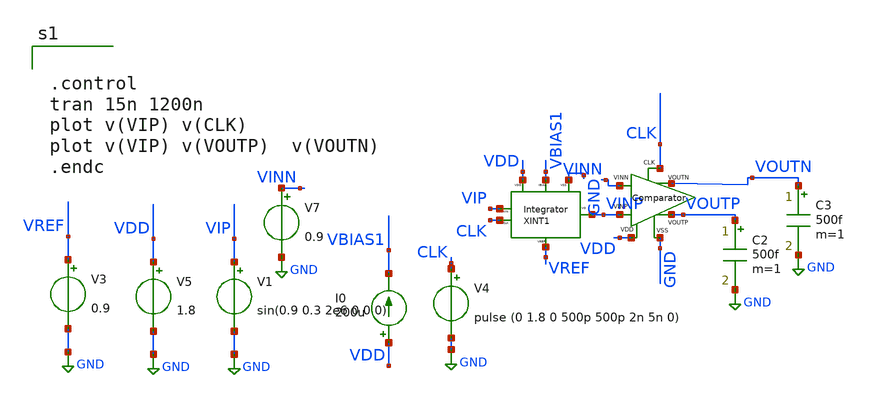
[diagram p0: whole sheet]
** sch_path: xschem/xschem_BGR_Top/Sigma_Delta/Integrator/Integrator_n_Comp_TB.sch
**.subckt Integrator_n_Comp_TB
V5 VDD GND 1.8
I0 VDD VBIAS1 200u
XINT1 VREF CLK VIP VINP VDD GND VBIAS1 Integrator
V3 VREF GND 0.9
V4 CLK GND pulse (0 1.8 0 500p 500p 2n 5n 0)
V1 VIP GND sin(0.9 0.3 2e6 0 0 0)
XCOMP1 VINN VINP VOUTN VOUTP CLK VDD GND Comparator
V7 VINN GND 0.9
C2 VOUTP GND 500f m=1
C3 VOUTN GND 500f m=1
**** begin user architecture code
** manual skywater pdks install (with patches applied)
* .lib $::SKYWATER_MODELS/models/sky130.lib.spice tt

** opencircuitdesign pdks install
.lib $::SKYWATER_MODELS/sky130.lib.spice tt




.control
tran 15n 1200n
plot v(VIP) v(CLK)
plot v(VIP) v(VOUTP)  v(VOUTN)
.endc

**** end user architecture code
**.ends

* expanding   symbol:  Sigma_Delta/Integrator/Integrator.sym # of pins=7
** sym_path: xschem/xschem_BGR_Top/Sigma_Delta/Integrator/Integrator.sym
** sch_path: xschem/xschem_BGR_Top/Sigma_Delta/Integrator/Integrator.sch
.subckt Integrator VREF CLK VIN VO VDD VSS IBIAS
*.iopin VDD
*.iopin VSS
*.iopin CLK
*.iopin IBIAS
*.iopin VREF
*.iopin VIN
*.iopin VO
XOpampM1 IBIAS VDD net1 VREF VSS VO OpampM
X1 VREF PH2 net1 VDD VSS PH1 VIN SC_Resistor
X2 PH2 VDD VSS PH1 CLK Non_over_clk
XC1 net1 VO sky130_fd_pr__cap_mim_m3_1 W=15 L=15 MF=1 m=1
.ends


* expanding   symbol:  Sigma_Delta/Comparator/Comparator.sym # of pins=7
** sym_path: xschem/xschem_BGR_Top/Sigma_Delta/Comparator/Comparator.sym
** sch_path: xschem/xschem_BGR_Top/Sigma_Delta/Comparator/Comparator.sch
.subckt Comparator VINN VINP VOUTN VOUTP CLK VDD VSS
*.iopin VDD
*.iopin VSS
*.iopin VOUTP
*.iopin VOUTN
*.iopin VINP
*.iopin VINN
*.iopin CLK
XM16 net1 net4 net2 VSS sky130_fd_pr__nfet_01v8 L=0.15 W=0.5 nf=1 ad='int((nf+1)/2) * W/nf * 0.29' as='int((nf+2)/2) * W/nf * 0.29'
+ pd='2*int((nf+1)/2) * (W/nf + 0.29)' ps='2*int((nf+2)/2) * (W/nf + 0.29)' nrd='0.29 / W' nrs='0.29 / W'
+ sa=0 sb=0 sd=0 mult=1 m=1
XM17 net1 net4 VDD VDD sky130_fd_pr__pfet_01v8 L=0.15 W=1 nf=1 ad='int((nf+1)/2) * W/nf * 0.29' as='int((nf+2)/2) * W/nf * 0.29'
+ pd='2*int((nf+1)/2) * (W/nf + 0.29)' ps='2*int((nf+2)/2) * (W/nf + 0.29)' nrd='0.29 / W' nrs='0.29 / W'
+ sa=0 sb=0 sd=0 mult=1 m=1
XM18 net2 VINN net3 VSS sky130_fd_pr__nfet_01v8 L=0.15 W=2 nf=1 ad='int((nf+1)/2) * W/nf * 0.29' as='int((nf+2)/2) * W/nf * 0.29'
+ pd='2*int((nf+1)/2) * (W/nf + 0.29)' ps='2*int((nf+2)/2) * (W/nf + 0.29)' nrd='0.29 / W' nrs='0.29 / W'
+ sa=0 sb=0 sd=0 mult=1 m=1
XM19 net1 CLK VDD VDD sky130_fd_pr__pfet_01v8 L=0.15 W=1 nf=1 ad='int((nf+1)/2) * W/nf * 0.29' as='int((nf+2)/2) * W/nf * 0.29'
+ pd='2*int((nf+1)/2) * (W/nf + 0.29)' ps='2*int((nf+2)/2) * (W/nf + 0.29)' nrd='0.29 / W' nrs='0.29 / W'
+ sa=0 sb=0 sd=0 mult=1 m=1
XM20 net2 CLK VDD VDD sky130_fd_pr__pfet_01v8 L=0.15 W=1 nf=1 ad='int((nf+1)/2) * W/nf * 0.29' as='int((nf+2)/2) * W/nf * 0.29'
+ pd='2*int((nf+1)/2) * (W/nf + 0.29)' ps='2*int((nf+2)/2) * (W/nf + 0.29)' nrd='0.29 / W' nrs='0.29 / W'
+ sa=0 sb=0 sd=0 mult=1 m=1
XM21 VOUTN net1 VSS VSS sky130_fd_pr__nfet_01v8 L=0.15 W=2 nf=1 ad='int((nf+1)/2) * W/nf * 0.29' as='int((nf+2)/2) * W/nf * 0.29'
+ pd='2*int((nf+1)/2) * (W/nf + 0.29)' ps='2*int((nf+2)/2) * (W/nf + 0.29)' nrd='0.29 / W' nrs='0.29 / W'
+ sa=0 sb=0 sd=0 mult=1 m=1
XM22 VOUTN net1 VDD VDD sky130_fd_pr__pfet_01v8 L=0.15 W=4 nf=1 ad='int((nf+1)/2) * W/nf * 0.29' as='int((nf+2)/2) * W/nf * 0.29'
+ pd='2*int((nf+1)/2) * (W/nf + 0.29)' ps='2*int((nf+2)/2) * (W/nf + 0.29)' nrd='0.29 / W' nrs='0.29 / W'
+ sa=0 sb=0 sd=0 mult=1 m=1
XM23 net4 net1 net5 VSS sky130_fd_pr__nfet_01v8 L=0.15 W=0.5 nf=1 ad='int((nf+1)/2) * W/nf * 0.29' as='int((nf+2)/2) * W/nf * 0.29'
+ pd='2*int((nf+1)/2) * (W/nf + 0.29)' ps='2*int((nf+2)/2) * (W/nf + 0.29)' nrd='0.29 / W' nrs='0.29 / W'
+ sa=0 sb=0 sd=0 mult=1 m=1
XM24 net4 net1 VDD VDD sky130_fd_pr__pfet_01v8 L=0.15 W=1 nf=1 ad='int((nf+1)/2) * W/nf * 0.29' as='int((nf+2)/2) * W/nf * 0.29'
+ pd='2*int((nf+1)/2) * (W/nf + 0.29)' ps='2*int((nf+2)/2) * (W/nf + 0.29)' nrd='0.29 / W' nrs='0.29 / W'
+ sa=0 sb=0 sd=0 mult=1 m=1
XM25 net5 VINP net3 VSS sky130_fd_pr__nfet_01v8 L=0.15 W=2 nf=1 ad='int((nf+1)/2) * W/nf * 0.29' as='int((nf+2)/2) * W/nf * 0.29'
+ pd='2*int((nf+1)/2) * (W/nf + 0.29)' ps='2*int((nf+2)/2) * (W/nf + 0.29)' nrd='0.29 / W' nrs='0.29 / W'
+ sa=0 sb=0 sd=0 mult=1 m=1
XM26 net4 CLK VDD VDD sky130_fd_pr__pfet_01v8 L=0.15 W=1 nf=1 ad='int((nf+1)/2) * W/nf * 0.29' as='int((nf+2)/2) * W/nf * 0.29'
+ pd='2*int((nf+1)/2) * (W/nf + 0.29)' ps='2*int((nf+2)/2) * (W/nf + 0.29)' nrd='0.29 / W' nrs='0.29 / W'
+ sa=0 sb=0 sd=0 mult=1 m=1
XM27 net5 CLK VDD VDD sky130_fd_pr__pfet_01v8 L=0.15 W=1 nf=1 ad='int((nf+1)/2) * W/nf * 0.29' as='int((nf+2)/2) * W/nf * 0.29'
+ pd='2*int((nf+1)/2) * (W/nf + 0.29)' ps='2*int((nf+2)/2) * (W/nf + 0.29)' nrd='0.29 / W' nrs='0.29 / W'
+ sa=0 sb=0 sd=0 mult=1 m=1
XM28 VOUTP net4 VSS VSS sky130_fd_pr__nfet_01v8 L=0.15 W=2 nf=1 ad='int((nf+1)/2) * W/nf * 0.29' as='int((nf+2)/2) * W/nf * 0.29'
+ pd='2*int((nf+1)/2) * (W/nf + 0.29)' ps='2*int((nf+2)/2) * (W/nf + 0.29)' nrd='0.29 / W' nrs='0.29 / W'
+ sa=0 sb=0 sd=0 mult=1 m=1
XM29 VOUTP net4 VDD VDD sky130_fd_pr__pfet_01v8 L=0.15 W=4 nf=1 ad='int((nf+1)/2) * W/nf * 0.29' as='int((nf+2)/2) * W/nf * 0.29'
+ pd='2*int((nf+1)/2) * (W/nf + 0.29)' ps='2*int((nf+2)/2) * (W/nf + 0.29)' nrd='0.29 / W' nrs='0.29 / W'
+ sa=0 sb=0 sd=0 mult=1 m=1
XM30 net3 CLK VSS VSS sky130_fd_pr__nfet_01v8 L=0.15 W=0.5 nf=1 ad='int((nf+1)/2) * W/nf * 0.29' as='int((nf+2)/2) * W/nf * 0.29'
+ pd='2*int((nf+1)/2) * (W/nf + 0.29)' ps='2*int((nf+2)/2) * (W/nf + 0.29)' nrd='0.29 / W' nrs='0.29 / W'
+ sa=0 sb=0 sd=0 mult=1 m=1
.ends


* expanding   symbol:  Sigma_Delta/Op_Amp/OpampM.sym # of pins=6
** sym_path: xschem/xschem_BGR_Top/Op_Amp/OpampM.sym
** sch_path: xschem/xschem_BGR_Top/Op_Amp/OpampM.sch
.subckt OpampM IBIAS VDD VN VP VSS VO
*.iopin VDD
*.iopin VSS
*.iopin VP
*.iopin VN
*.iopin VO
*.iopin IBIAS
XM1 net1 VN net3 VSS sky130_fd_pr__nfet_01v8 L=0.5 W=50 nf=10 ad='int((nf+1)/2) * W/nf * 0.29' as='int((nf+2)/2) * W/nf * 0.29'
+ pd='2*int((nf+1)/2) * (W/nf + 0.29)' ps='2*int((nf+2)/2) * (W/nf + 0.29)' nrd='0.29 / W' nrs='0.29 / W'
+ sa=0 sb=0 sd=0 mult=1 m=1
XM3 net1 net1 VDD VDD sky130_fd_pr__pfet_01v8_lvt L=0.5 W=60 nf=10 ad='int((nf+1)/2) * W/nf * 0.29' as='int((nf+2)/2) * W/nf * 0.29'
+ pd='2*int((nf+1)/2) * (W/nf + 0.29)' ps='2*int((nf+2)/2) * (W/nf + 0.29)' nrd='0.29 / W' nrs='0.29 / W'
+ sa=0 sb=0 sd=0 mult=1 m=1
XM2 net2 VP net3 VSS sky130_fd_pr__nfet_01v8 L=0.5 W=50 nf=10 ad='int((nf+1)/2) * W/nf * 0.29' as='int((nf+2)/2) * W/nf * 0.29'
+ pd='2*int((nf+1)/2) * (W/nf + 0.29)' ps='2*int((nf+2)/2) * (W/nf + 0.29)' nrd='0.29 / W' nrs='0.29 / W'
+ sa=0 sb=0 sd=0 mult=1 m=1
XM4 net2 net1 VDD VDD sky130_fd_pr__pfet_01v8_lvt L=0.5 W=60 nf=10 ad='int((nf+1)/2) * W/nf * 0.29' as='int((nf+2)/2) * W/nf * 0.29'
+ pd='2*int((nf+1)/2) * (W/nf + 0.29)' ps='2*int((nf+2)/2) * (W/nf + 0.29)' nrd='0.29 / W' nrs='0.29 / W'
+ sa=0 sb=0 sd=0 mult=1 m=1
XM5 net3 IBIAS VSS VSS sky130_fd_pr__nfet_01v8 L=0.5 W=21 nf=10 ad='int((nf+1)/2) * W/nf * 0.29' as='int((nf+2)/2) * W/nf * 0.29'
+ pd='2*int((nf+1)/2) * (W/nf + 0.29)' ps='2*int((nf+2)/2) * (W/nf + 0.29)' nrd='0.29 / W' nrs='0.29 / W'
+ sa=0 sb=0 sd=0 mult=1 m=1
XM7 VO IBIAS VSS VSS sky130_fd_pr__nfet_01v8 L=0.5 W=63 nf=10 ad='int((nf+1)/2) * W/nf * 0.29' as='int((nf+2)/2) * W/nf * 0.29'
+ pd='2*int((nf+1)/2) * (W/nf + 0.29)' ps='2*int((nf+2)/2) * (W/nf + 0.29)' nrd='0.29 / W' nrs='0.29 / W'
+ sa=0 sb=0 sd=0 mult=1 m=1
XM8 IBIAS IBIAS VSS VSS sky130_fd_pr__nfet_01v8 L=0.5 W=21 nf=10 ad='int((nf+1)/2) * W/nf * 0.29' as='int((nf+2)/2) * W/nf * 0.29'
+ pd='2*int((nf+1)/2) * (W/nf + 0.29)' ps='2*int((nf+2)/2) * (W/nf + 0.29)' nrd='0.29 / W' nrs='0.29 / W'
+ sa=0 sb=0 sd=0 mult=1 m=1
XC1 net2 VO sky130_fd_pr__cap_mim_m3_1 W=24 L=24 MF=1 m=1
XC2 VDD VSS sky130_fd_pr__cap_mim_m3_1 W=30 L=10 MF=1 m=1
XC3 VDD VSS sky130_fd_pr__cap_mim_m3_1 W=30 L=10 MF=1 m=1
XM6 VO net2 VDD VDD sky130_fd_pr__pfet_01v8_lvt L=0.50 W=355 nf=20 ad='int((nf+1)/2) * W/nf * 0.29' as='int((nf+2)/2) * W/nf * 0.29'
+ pd='2*int((nf+1)/2) * (W/nf + 0.29)' ps='2*int((nf+2)/2) * (W/nf + 0.29)' nrd='0.29 / W' nrs='0.29 / W'
+ sa=0 sb=0 sd=0 mult=1 m=1
.ends


* expanding   symbol:  Sigma_Delta/SC_Resistor/SC_Resistor.sym # of pins=7
** sym_path: xschem/xschem_BGR_Top/Sigma_Delta/SC_Resistor/SC_Resistor.sym
** sch_path: xschem/xschem_BGR_Top/Sigma_Delta/SC_Resistor/SC_Resistor.sch
.subckt SC_Resistor VREF PH2 VOUT VDD VSS PH1 VIN
*.iopin VDD
*.iopin PH1
*.iopin VIN
*.iopin VOUT
*.iopin PH2
*.iopin VREF
*.iopin VSS
XTG3 VSS PH1 VDD VIN MID1 TG
XTG4 VSS PH2 VDD MID2 VOUT TG
XM2 MID1 PH2 VREF VSS sky130_fd_pr__nfet_01v8 L=0.15 W=20 nf=2 ad='int((nf+1)/2) * W/nf * 0.29' as='int((nf+2)/2) * W/nf * 0.29'
+ pd='2*int((nf+1)/2) * (W/nf + 0.29)' ps='2*int((nf+2)/2) * (W/nf + 0.29)' nrd='0.29 / W' nrs='0.29 / W'
+ sa=0 sb=0 sd=0 mult=1 m=1
XM1 MID2 PH1 VREF VSS sky130_fd_pr__nfet_01v8 L=0.15 W=20 nf=2 ad='int((nf+1)/2) * W/nf * 0.29' as='int((nf+2)/2) * W/nf * 0.29'
+ pd='2*int((nf+1)/2) * (W/nf + 0.29)' ps='2*int((nf+2)/2) * (W/nf + 0.29)' nrd='0.29 / W' nrs='0.29 / W'
+ sa=0 sb=0 sd=0 mult=1 m=1
XC2 MID2 MID1 sky130_fd_pr__cap_mim_m3_2 W=32 L=32 MF=1 m=1
.ends


* expanding   symbol:  Sigma_Delta/Non_over_clk/Non_over_clk.sym # of pins=5
** sym_path: xschem/xschem_BGR_Top/Sigma_Delta/Non_over_clk/Non_over_clk.sym
** sch_path: xschem/xschem_BGR_Top/Sigma_Delta/Non_over_clk/Non_over_clk.sch
.subckt Non_over_clk PH2 VDD VSS PH1 CLK
*.iopin VDD
*.iopin VSS
*.iopin CLK
*.iopin PH1
*.iopin PH2
X1 VSS VDD CLK net1 Inverter
X2 VSS VDD net9 PH1 Inverter
X3 VSS VDD net8 PH2 Inverter
X4 VSS VDD net3 net2 INV_1x64
X5 VSS VDD net5 net4 INV_1x64
XNOR1 VDD VSS net1 PH2 net3 NOR
XNOR2 VDD VSS CLK PH1 net5 NOR
X8 VSS VDD net6 net8 Inverter
X9 VSS VDD net7 net9 Inverter
X6 VSS VDD net2 net7 INV_1x64
X7 VSS VDD net4 net6 INV_1x64
.ends


* expanding   symbol:  Sigma_Delta/Transmission_Gate/TG.sym # of pins=5
** sym_path: xschem/xschem_BGR_Top/Sigma_Delta/Transmission_Gate/TG.sym
** sch_path: xschem/xschem_BGR_Top/Sigma_Delta/Transmission_Gate/TG.sch
.subckt TG VSS CLK VDD A B
*.iopin VDD
*.iopin VSS
*.iopin A
*.iopin B
*.iopin CLK
XM1 A CLK B VSS sky130_fd_pr__nfet_01v8 L=0.15 W=10 nf=1 ad='int((nf+1)/2) * W/nf * 0.29' as='int((nf+2)/2) * W/nf * 0.29'
+ pd='2*int((nf+1)/2) * (W/nf + 0.29)' ps='2*int((nf+2)/2) * (W/nf + 0.29)' nrd='0.29 / W' nrs='0.29 / W'
+ sa=0 sb=0 sd=0 mult=1 m=1
XM2 B CLKB A VDD sky130_fd_pr__pfet_01v8 L=0.15 W=20 nf=2 ad='int((nf+1)/2) * W/nf * 0.29' as='int((nf+2)/2) * W/nf * 0.29'
+ pd='2*int((nf+1)/2) * (W/nf + 0.29)' ps='2*int((nf+2)/2) * (W/nf + 0.29)' nrd='0.29 / W' nrs='0.29 / W'
+ sa=0 sb=0 sd=0 mult=1 m=1
XM3 CLKB CLK VSS VSS sky130_fd_pr__nfet_01v8 L=0.15 W=10 nf=5 ad='int((nf+1)/2) * W/nf * 0.29' as='int((nf+2)/2) * W/nf * 0.29'
+ pd='2*int((nf+1)/2) * (W/nf + 0.29)' ps='2*int((nf+2)/2) * (W/nf + 0.29)' nrd='0.29 / W' nrs='0.29 / W'
+ sa=0 sb=0 sd=0 mult=1 m=1
XM4 CLKB CLK VDD VDD sky130_fd_pr__pfet_01v8 L=0.15 W=20 nf=10 ad='int((nf+1)/2) * W/nf * 0.29' as='int((nf+2)/2) * W/nf * 0.29'
+ pd='2*int((nf+1)/2) * (W/nf + 0.29)' ps='2*int((nf+2)/2) * (W/nf + 0.29)' nrd='0.29 / W' nrs='0.29 / W'
+ sa=0 sb=0 sd=0 mult=1 m=1
.ends


* expanding   symbol:  Sigma_Delta/Inverter/Inverter.sym # of pins=4
** sym_path: xschem/xschem_BGR_Top/Sigma_Delta/Inverter/Inverter.sym
** sch_path: xschem/xschem_BGR_Top/Sigma_Delta/Inverter/Inverter.sch
.subckt Inverter VSS VDD VIN VOUT
*.ipin VIN
*.iopin VDD
*.iopin VSS
*.opin VOUT
XM1 VOUT VIN VSS VSS sky130_fd_pr__nfet_01v8 L=0.15 W=0.9 nf=1 ad='int((nf+1)/2) * W/nf * 0.29' as='int((nf+2)/2) * W/nf * 0.29'
+ pd='2*int((nf+1)/2) * (W/nf + 0.29)' ps='2*int((nf+2)/2) * (W/nf + 0.29)' nrd='0.29 / W' nrs='0.29 / W'
+ sa=0 sb=0 sd=0 mult=1 m=1
XM2 VOUT VIN VDD VDD sky130_fd_pr__pfet_01v8 L=0.15 W=0.9 nf=2 ad='int((nf+1)/2) * W/nf * 0.29' as='int((nf+2)/2) * W/nf * 0.29'
+ pd='2*int((nf+1)/2) * (W/nf + 0.29)' ps='2*int((nf+2)/2) * (W/nf + 0.29)' nrd='0.29 / W' nrs='0.29 / W'
+ sa=0 sb=0 sd=0 mult=1 m=1
.ends


* expanding   symbol:  Sigma_Delta/INV_1x64/INV_1x64.sym # of pins=4
** sym_path: xschem/xschem_BGR_Top/Sigma_Delta/INV_1x64/INV_1x64.sym
** sch_path: xschem/xschem_BGR_Top/Sigma_Delta/INV_1x64/INV_1x64.sch
.subckt INV_1x64 VSS VDD VIN VOUT
*.ipin VIN
*.iopin VDD
*.iopin VSS
*.opin VOUT
XM1 VOUT VIN net1 VSS sky130_fd_pr__nfet_01v8 L=0.15 W=0.425 nf=1 ad='int((nf+1)/2) * W/nf * 0.29' as='int((nf+2)/2) * W/nf * 0.29'
+ pd='2*int((nf+1)/2) * (W/nf + 0.29)' ps='2*int((nf+2)/2) * (W/nf + 0.29)' nrd='0.29 / W' nrs='0.29 / W'
+ sa=0 sb=0 sd=0 mult=1 m=1
XM2 VOUT VIN net2 VDD sky130_fd_pr__pfet_01v8 L=0.15 W=0.425 nf=1 ad='int((nf+1)/2) * W/nf * 0.29' as='int((nf+2)/2) * W/nf * 0.29'
+ pd='2*int((nf+1)/2) * (W/nf + 0.29)' ps='2*int((nf+2)/2) * (W/nf + 0.29)' nrd='0.29 / W' nrs='0.29 / W'
+ sa=0 sb=0 sd=0 mult=1 m=1
XM3 net2 VIN net3 VDD sky130_fd_pr__pfet_01v8 L=0.15 W=0.425 nf=1 ad='int((nf+1)/2) * W/nf * 0.29' as='int((nf+2)/2) * W/nf * 0.29'
+ pd='2*int((nf+1)/2) * (W/nf + 0.29)' ps='2*int((nf+2)/2) * (W/nf + 0.29)' nrd='0.29 / W' nrs='0.29 / W'
+ sa=0 sb=0 sd=0 mult=1 m=1
XM4 net3 VIN net4 VDD sky130_fd_pr__pfet_01v8 L=0.15 W=0.425 nf=1 ad='int((nf+1)/2) * W/nf * 0.29' as='int((nf+2)/2) * W/nf * 0.29'
+ pd='2*int((nf+1)/2) * (W/nf + 0.29)' ps='2*int((nf+2)/2) * (W/nf + 0.29)' nrd='0.29 / W' nrs='0.29 / W'
+ sa=0 sb=0 sd=0 mult=1 m=1
XM5 net4 VIN net8 VDD sky130_fd_pr__pfet_01v8 L=0.15 W=0.425 nf=1 ad='int((nf+1)/2) * W/nf * 0.29' as='int((nf+2)/2) * W/nf * 0.29'
+ pd='2*int((nf+1)/2) * (W/nf + 0.29)' ps='2*int((nf+2)/2) * (W/nf + 0.29)' nrd='0.29 / W' nrs='0.29 / W'
+ sa=0 sb=0 sd=0 mult=1 m=1
XM6 net1 VIN net5 VSS sky130_fd_pr__nfet_01v8 L=0.15 W=0.425 nf=1 ad='int((nf+1)/2) * W/nf * 0.29' as='int((nf+2)/2) * W/nf * 0.29'
+ pd='2*int((nf+1)/2) * (W/nf + 0.29)' ps='2*int((nf+2)/2) * (W/nf + 0.29)' nrd='0.29 / W' nrs='0.29 / W'
+ sa=0 sb=0 sd=0 mult=1 m=1
XM7 net5 VIN net6 VSS sky130_fd_pr__nfet_01v8 L=0.15 W=0.425 nf=1 ad='int((nf+1)/2) * W/nf * 0.29' as='int((nf+2)/2) * W/nf * 0.29'
+ pd='2*int((nf+1)/2) * (W/nf + 0.29)' ps='2*int((nf+2)/2) * (W/nf + 0.29)' nrd='0.29 / W' nrs='0.29 / W'
+ sa=0 sb=0 sd=0 mult=1 m=1
XM8 net6 VIN net7 VSS sky130_fd_pr__nfet_01v8 L=0.15 W=0.425 nf=1 ad='int((nf+1)/2) * W/nf * 0.29' as='int((nf+2)/2) * W/nf * 0.29'
+ pd='2*int((nf+1)/2) * (W/nf + 0.29)' ps='2*int((nf+2)/2) * (W/nf + 0.29)' nrd='0.29 / W' nrs='0.29 / W'
+ sa=0 sb=0 sd=0 mult=1 m=1
XM9 net7 VIN VSS VSS sky130_fd_pr__nfet_01v8 L=0.15 W=0.425 nf=1 ad='int((nf+1)/2) * W/nf * 0.29' as='int((nf+2)/2) * W/nf * 0.29'
+ pd='2*int((nf+1)/2) * (W/nf + 0.29)' ps='2*int((nf+2)/2) * (W/nf + 0.29)' nrd='0.29 / W' nrs='0.29 / W'
+ sa=0 sb=0 sd=0 mult=1 m=1
XM10 net8 VIN VDD VDD sky130_fd_pr__pfet_01v8 L=0.15 W=0.425 nf=1 ad='int((nf+1)/2) * W/nf * 0.29' as='int((nf+2)/2) * W/nf * 0.29'
+ pd='2*int((nf+1)/2) * (W/nf + 0.29)' ps='2*int((nf+2)/2) * (W/nf + 0.29)' nrd='0.29 / W' nrs='0.29 / W'
+ sa=0 sb=0 sd=0 mult=1 m=1
.ends


* expanding   symbol:  Sigma_Delta/Nor/NOR.sym # of pins=5
** sym_path: xschem/xschem_BGR_Top/Sigma_Delta/Nor/NOR.sym
** sch_path: xschem/xschem_BGR_Top/Sigma_Delta/Nor/NOR.sch
.subckt NOR VDD VSS A B OUT
*.iopin VDD
*.iopin VSS
*.iopin A
*.iopin B
*.iopin OUT
XM2 OUT A VSS VSS sky130_fd_pr__nfet_01v8 L=0.15 W=0.5 nf=1 ad='int((nf+1)/2) * W/nf * 0.29' as='int((nf+2)/2) * W/nf * 0.29'
+ pd='2*int((nf+1)/2) * (W/nf + 0.29)' ps='2*int((nf+2)/2) * (W/nf + 0.29)' nrd='0.29 / W' nrs='0.29 / W'
+ sa=0 sb=0 sd=0 mult=1 m=1
XM3 net1 A VDD VDD sky130_fd_pr__pfet_01v8 L=0.15 W=0.5 nf=1 ad='int((nf+1)/2) * W/nf * 0.29' as='int((nf+2)/2) * W/nf * 0.29'
+ pd='2*int((nf+1)/2) * (W/nf + 0.29)' ps='2*int((nf+2)/2) * (W/nf + 0.29)' nrd='0.29 / W' nrs='0.29 / W'
+ sa=0 sb=0 sd=0 mult=1 m=1
XM1 OUT B net1 VDD sky130_fd_pr__pfet_01v8 L=0.15 W=0.5 nf=1 ad='int((nf+1)/2) * W/nf * 0.29' as='int((nf+2)/2) * W/nf * 0.29'
+ pd='2*int((nf+1)/2) * (W/nf + 0.29)' ps='2*int((nf+2)/2) * (W/nf + 0.29)' nrd='0.29 / W' nrs='0.29 / W'
+ sa=0 sb=0 sd=0 mult=1 m=1
XM4 OUT B VSS VSS sky130_fd_pr__nfet_01v8 L=0.15 W=0.5 nf=1 ad='int((nf+1)/2) * W/nf * 0.29' as='int((nf+2)/2) * W/nf * 0.29'
+ pd='2*int((nf+1)/2) * (W/nf + 0.29)' ps='2*int((nf+2)/2) * (W/nf + 0.29)' nrd='0.29 / W' nrs='0.29 / W'
+ sa=0 sb=0 sd=0 mult=1 m=1
.ends

.GLOBAL GND
.end
